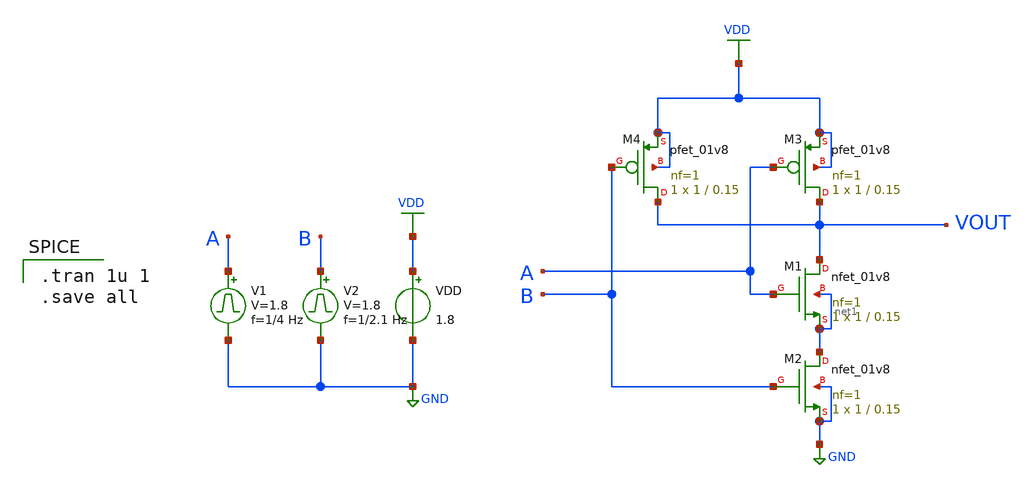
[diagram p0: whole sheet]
** sch_path: Circuits/Examples/Digital/NAND/NAND_gate.sch
**.subckt NAND_gate
VDD VDD GND 1.8
XM1 VOUT A net1 net1 sky130_fd_pr__nfet_01v8 L=0.15 W=1 nf=1 ad='int((nf+1)/2) * W/nf * 0.29' as='int((nf+2)/2) * W/nf * 0.29'
+ pd='2*int((nf+1)/2) * (W/nf + 0.29)' ps='2*int((nf+2)/2) * (W/nf + 0.29)' nrd='0.29 / W' nrs='0.29 / W'
+ sa=0 sb=0 sd=0 mult=1 m=1
XM2 net1 B GND GND sky130_fd_pr__nfet_01v8 L=0.15 W=1 nf=1 ad='int((nf+1)/2) * W/nf * 0.29' as='int((nf+2)/2) * W/nf * 0.29'
+ pd='2*int((nf+1)/2) * (W/nf + 0.29)' ps='2*int((nf+2)/2) * (W/nf + 0.29)' nrd='0.29 / W' nrs='0.29 / W'
+ sa=0 sb=0 sd=0 mult=1 m=1
XM3 VOUT A VDD VDD sky130_fd_pr__pfet_01v8 L=0.15 W=1 nf=1 ad='int((nf+1)/2) * W/nf * 0.29' as='int((nf+2)/2) * W/nf * 0.29'
+ pd='2*int((nf+1)/2) * (W/nf + 0.29)' ps='2*int((nf+2)/2) * (W/nf + 0.29)' nrd='0.29 / W' nrs='0.29 / W'
+ sa=0 sb=0 sd=0 mult=1 m=1
XM4 VOUT B VDD VDD sky130_fd_pr__pfet_01v8 L=0.15 W=1 nf=1 ad='int((nf+1)/2) * W/nf * 0.29' as='int((nf+2)/2) * W/nf * 0.29'
+ pd='2*int((nf+1)/2) * (W/nf + 0.29)' ps='2*int((nf+2)/2) * (W/nf + 0.29)' nrd='0.29 / W' nrs='0.29 / W'
+ sa=0 sb=0 sd=0 mult=1 m=1
V1 A GND pulse 0 1.8 '0.495/ 1/4 ' '0.01/1/4 ' '0.01/1/4 ' '0.49/1/4 ' '1/1/4 '
V2 B GND pulse 0 1.8 '0.495/ 1/2.1 ' '0.01/1/2.1 ' '0.01/1/2.1 ' '0.49/1/2.1 ' '1/1/2.1 '
**** begin user architecture code
 ** manual skywater pdks install (with patches applied)
* .lib $::SKYWATER_MODELS/models/sky130.lib.spice tt

** opencircuitdesign pdks install
.lib $::SKYWATER_MODELS/sky130.lib.spice tt

.param mc_mm_switch=0
.param mc_pr_switch=0


.tran 1u 1
.save all

**** end user architecture code
**.ends
.GLOBAL VDD
.GLOBAL GND
.end
